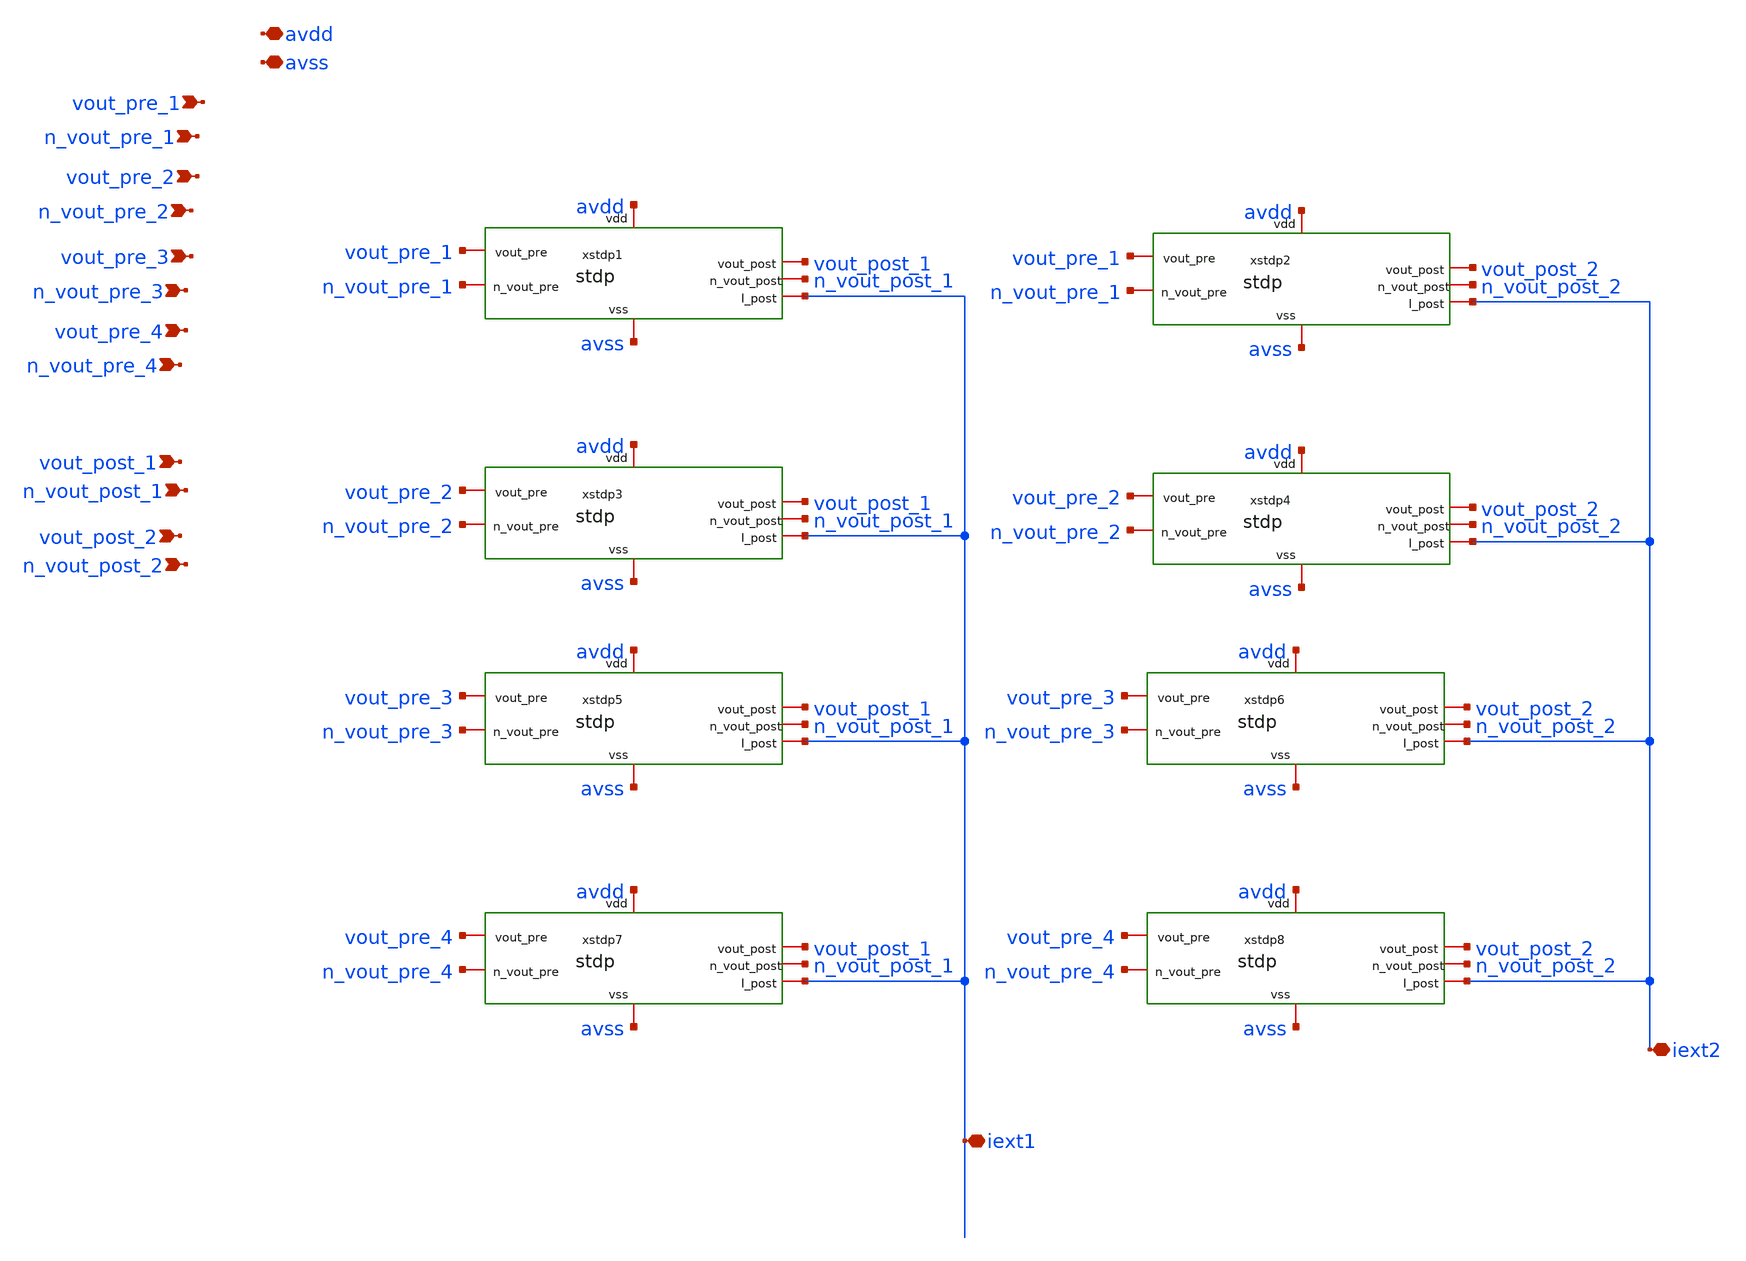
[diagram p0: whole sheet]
** sch_path: Synapse/stdp_4x2.sch
**.subckt stdp_4x2 avdd avss vout_pre_1 n_vout_pre_1 vout_pre_2 n_vout_pre_2 vout_pre_3 n_vout_pre_3
*+ vout_pre_4 n_vout_pre_4 n_vout_post_1 vout_post_1 n_vout_post_2 vout_post_2 iext1 iext2
*.iopin avdd
*.iopin avss
*.ipin vout_pre_1
*.ipin n_vout_pre_1
*.ipin vout_pre_2
*.ipin n_vout_pre_2
*.ipin vout_pre_3
*.ipin n_vout_pre_3
*.ipin vout_pre_4
*.ipin n_vout_pre_4
*.ipin n_vout_post_1
*.ipin vout_post_1
*.ipin n_vout_post_2
*.ipin vout_post_2
*.iopin iext1
*.iopin iext2
xstdp1 avdd avss vout_pre_1 vout_post_1 iext1 n_vout_pre_1 n_vout_post_1 stdp
xstdp2 avdd avss vout_pre_1 vout_post_2 iext2 n_vout_pre_1 n_vout_post_2 stdp
xstdp3 avdd avss vout_pre_2 vout_post_1 iext1 n_vout_pre_2 n_vout_post_1 stdp
xstdp4 avdd avss vout_pre_2 vout_post_2 iext2 n_vout_pre_2 n_vout_post_2 stdp
xstdp5 avdd avss vout_pre_3 vout_post_1 iext1 n_vout_pre_3 n_vout_post_1 stdp
xstdp6 avdd avss vout_pre_3 vout_post_2 iext2 n_vout_pre_3 n_vout_post_2 stdp
xstdp7 avdd avss vout_pre_4 vout_post_1 iext1 n_vout_pre_4 n_vout_post_1 stdp
xstdp8 avdd avss vout_pre_4 vout_post_2 iext2 n_vout_pre_4 n_vout_post_2 stdp
**.ends

* expanding   symbol:  /foss/designs/SNN_IPN/Synapse/stdp.sym # of pins=7
** sym_path: Synapse/stdp.sym
** sch_path: Synapse/stdp.sch
.subckt stdp vdd vss vout_pre vout_post I_post n_vout_pre n_vout_post
*.iopin vdd
*.iopin vss
*.iopin vout_post
*.iopin vout_pre
*.iopin I_post
*.iopin n_vout_pre
*.iopin n_vout_post
XM3 be vout_post vss vss sky130_fd_pr__nfet_01v8 L=0.15 W=5 nf=1 ad='int((nf+1)/2) * W/nf * 0.29' as='int((nf+2)/2) * W/nf * 0.29'
+ pd='2*int((nf+1)/2) * (W/nf + 0.29)' ps='2*int((nf+2)/2) * (W/nf + 0.29)' nrd='0.29 / W' nrs='0.29 / W'
+ sa=0 sb=0 sd=0 mult=1 m=1
XM4 net1 vout_pre vss vss sky130_fd_pr__nfet_01v8 L=0.15 W=5 nf=1 ad='int((nf+1)/2) * W/nf * 0.29' as='int((nf+2)/2) * W/nf * 0.29'
+ pd='2*int((nf+1)/2) * (W/nf + 0.29)' ps='2*int((nf+2)/2) * (W/nf + 0.29)' nrd='0.29 / W' nrs='0.29 / W'
+ sa=0 sb=0 sd=0 mult=1 m=1
XR2 te be rram_v0
XM14 net3 net2 vdd vdd sky130_fd_pr__pfet_01v8 L=0.15 W=1 nf=1 ad='int((nf+1)/2) * W/nf * 0.29' as='int((nf+2)/2) * W/nf * 0.29'
+ pd='2*int((nf+1)/2) * (W/nf + 0.29)' ps='2*int((nf+2)/2) * (W/nf + 0.29)' nrd='0.29 / W' nrs='0.29 / W'
+ sa=0 sb=0 sd=0 mult=1 m=1
XM15 net2 net2 vdd vdd sky130_fd_pr__pfet_01v8 L=0.15 W=10 nf=1 ad='int((nf+1)/2) * W/nf * 0.29' as='int((nf+2)/2) * W/nf * 0.29'
+ pd='2*int((nf+1)/2) * (W/nf + 0.29)' ps='2*int((nf+2)/2) * (W/nf + 0.29)' nrd='0.29 / W' nrs='0.29 / W'
+ sa=0 sb=0 sd=0 mult=1 m=1
**** begin user architecture code


.save v(te) v(be) i(vmr)


**** end user architecture code
Vmr te net1 0
.save i(vmr)
XM1 net1 n_vout_post net2 vss sky130_fd_pr__pfet_01v8 L=0.15 W=10 nf=1 ad='int((nf+1)/2) * W/nf * 0.29'
+ as='int((nf+2)/2) * W/nf * 0.29' pd='2*int((nf+1)/2) * (W/nf + 0.29)' ps='2*int((nf+2)/2) * (W/nf + 0.29)'
+ nrd='0.29 / W' nrs='0.29 / W' sa=0 sb=0 sd=0 mult=1 m=1
XM2 be n_vout_pre net2 vss sky130_fd_pr__pfet_01v8 L=0.15 W=10 nf=1 ad='int((nf+1)/2) * W/nf * 0.29'
+ as='int((nf+2)/2) * W/nf * 0.29' pd='2*int((nf+1)/2) * (W/nf + 0.29)' ps='2*int((nf+2)/2) * (W/nf + 0.29)'
+ nrd='0.29 / W' nrs='0.29 / W' sa=0 sb=0 sd=0 mult=1 m=1
XM6 I_post net2 net3 vdd sky130_fd_pr__pfet_01v8 L=0.15 W=1 nf=1 ad='int((nf+1)/2) * W/nf * 0.29' as='int((nf+2)/2) * W/nf * 0.29'
+ pd='2*int((nf+1)/2) * (W/nf + 0.29)' ps='2*int((nf+2)/2) * (W/nf + 0.29)' nrd='0.29 / W' nrs='0.29 / W'
+ sa=0 sb=0 sd=0 mult=1 m=1
.ends

.end
